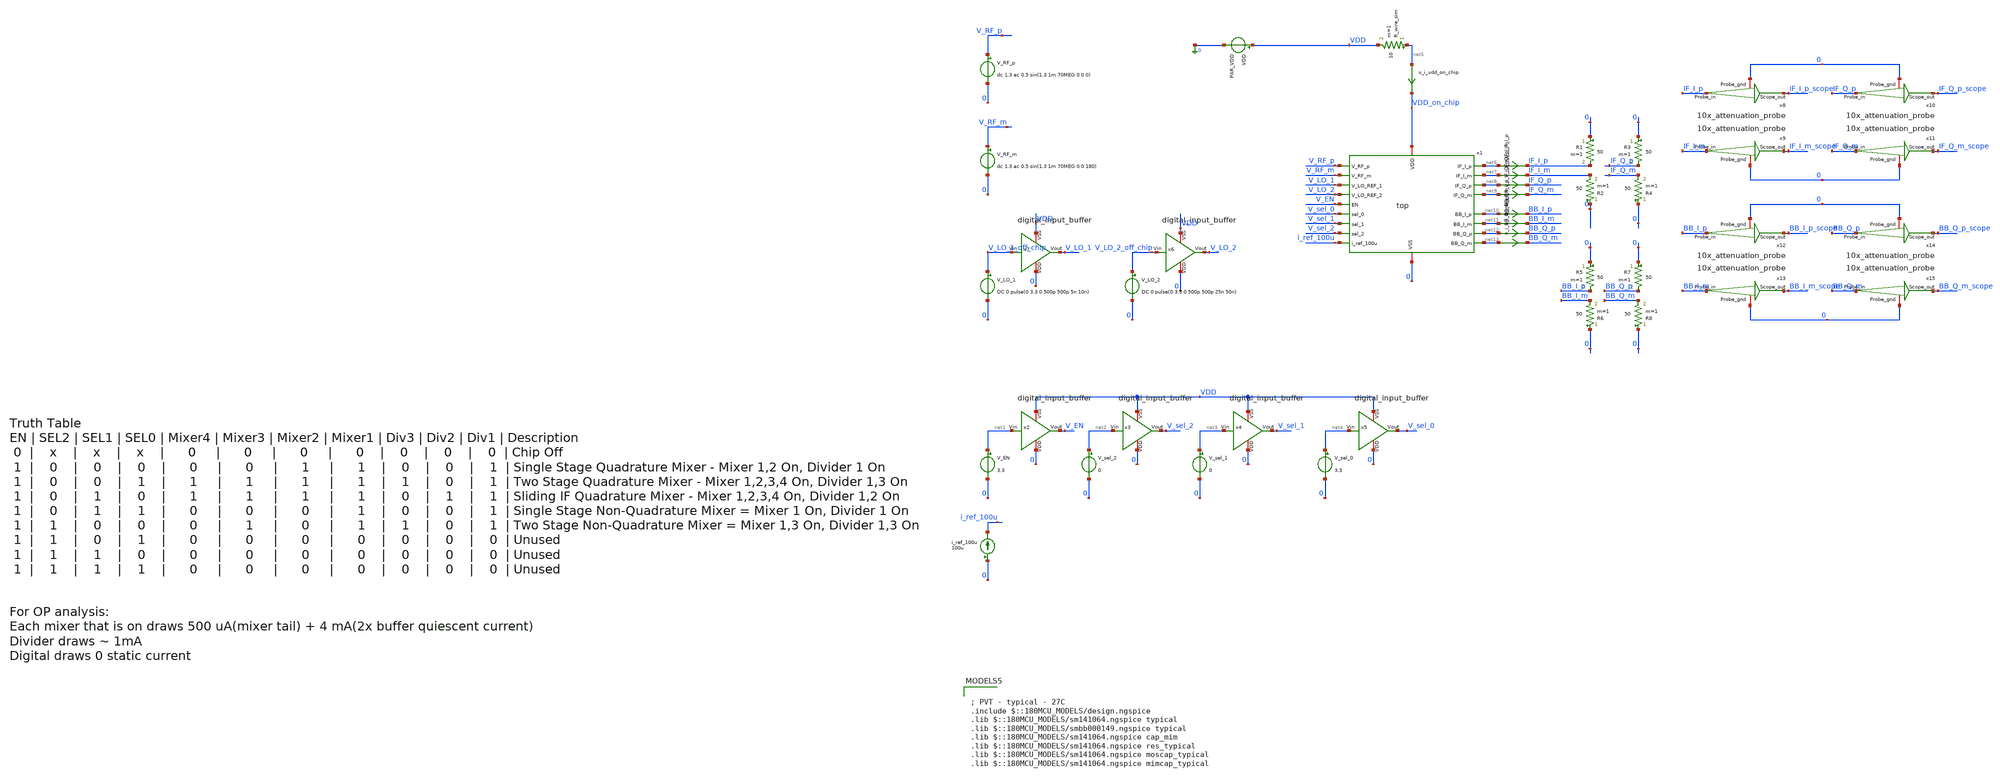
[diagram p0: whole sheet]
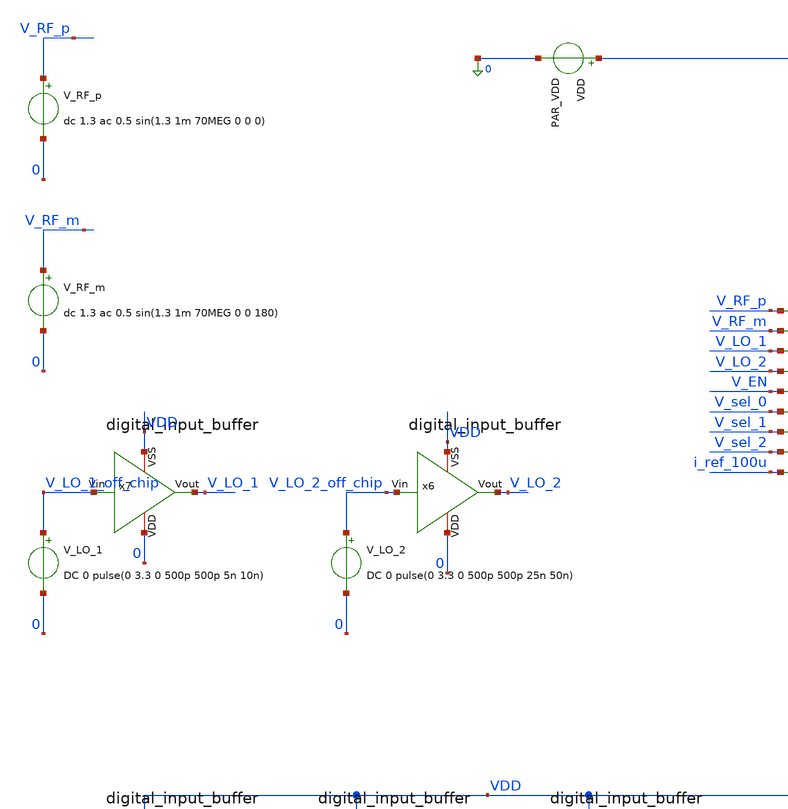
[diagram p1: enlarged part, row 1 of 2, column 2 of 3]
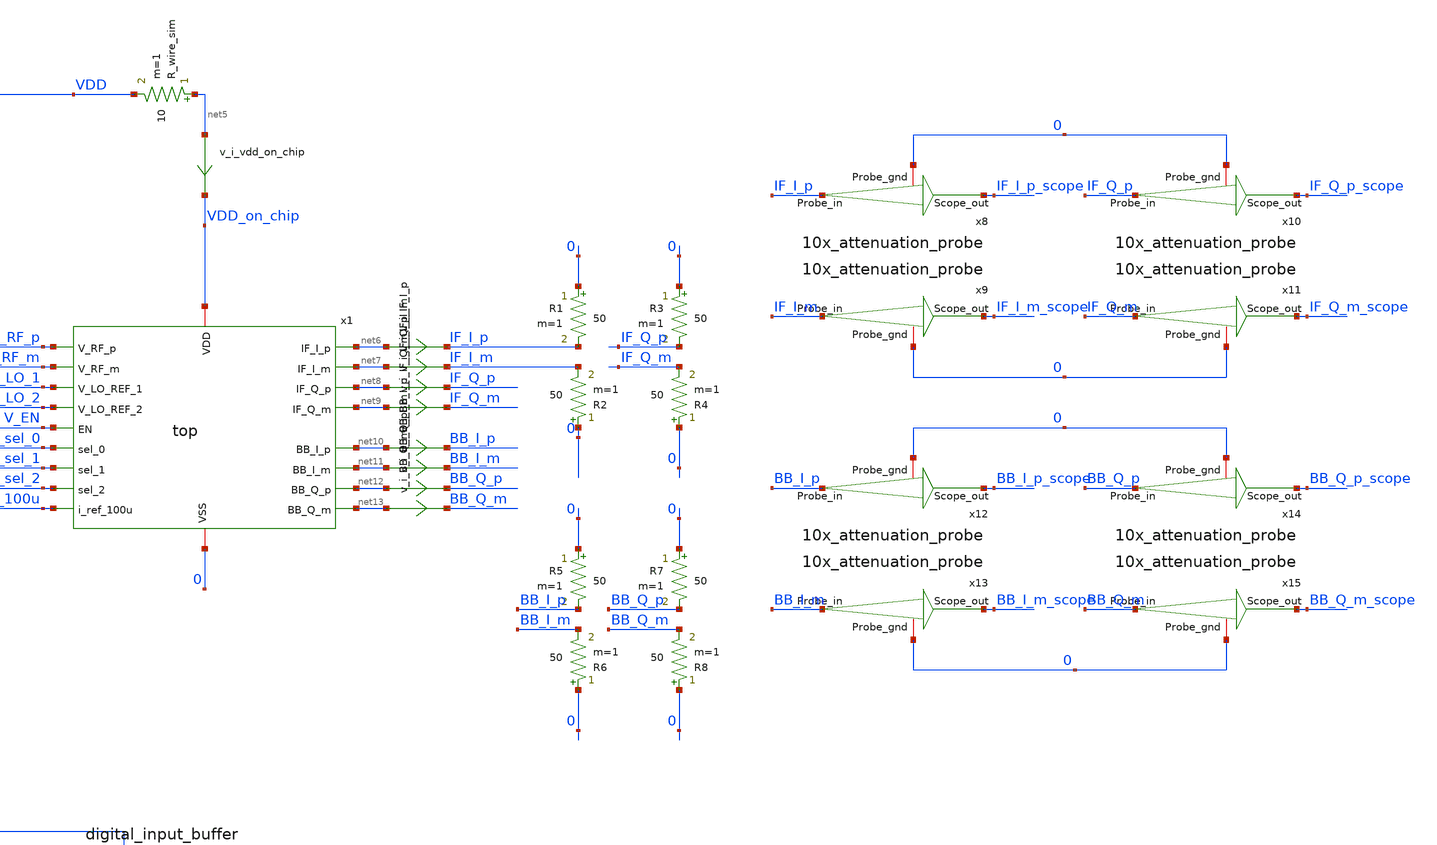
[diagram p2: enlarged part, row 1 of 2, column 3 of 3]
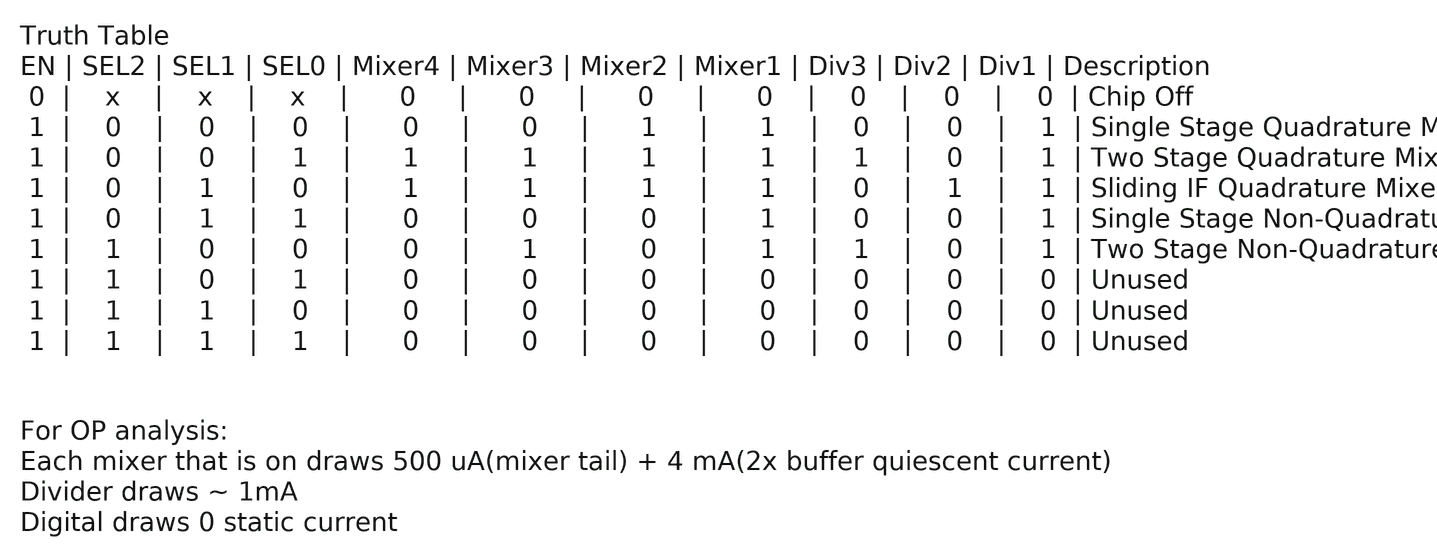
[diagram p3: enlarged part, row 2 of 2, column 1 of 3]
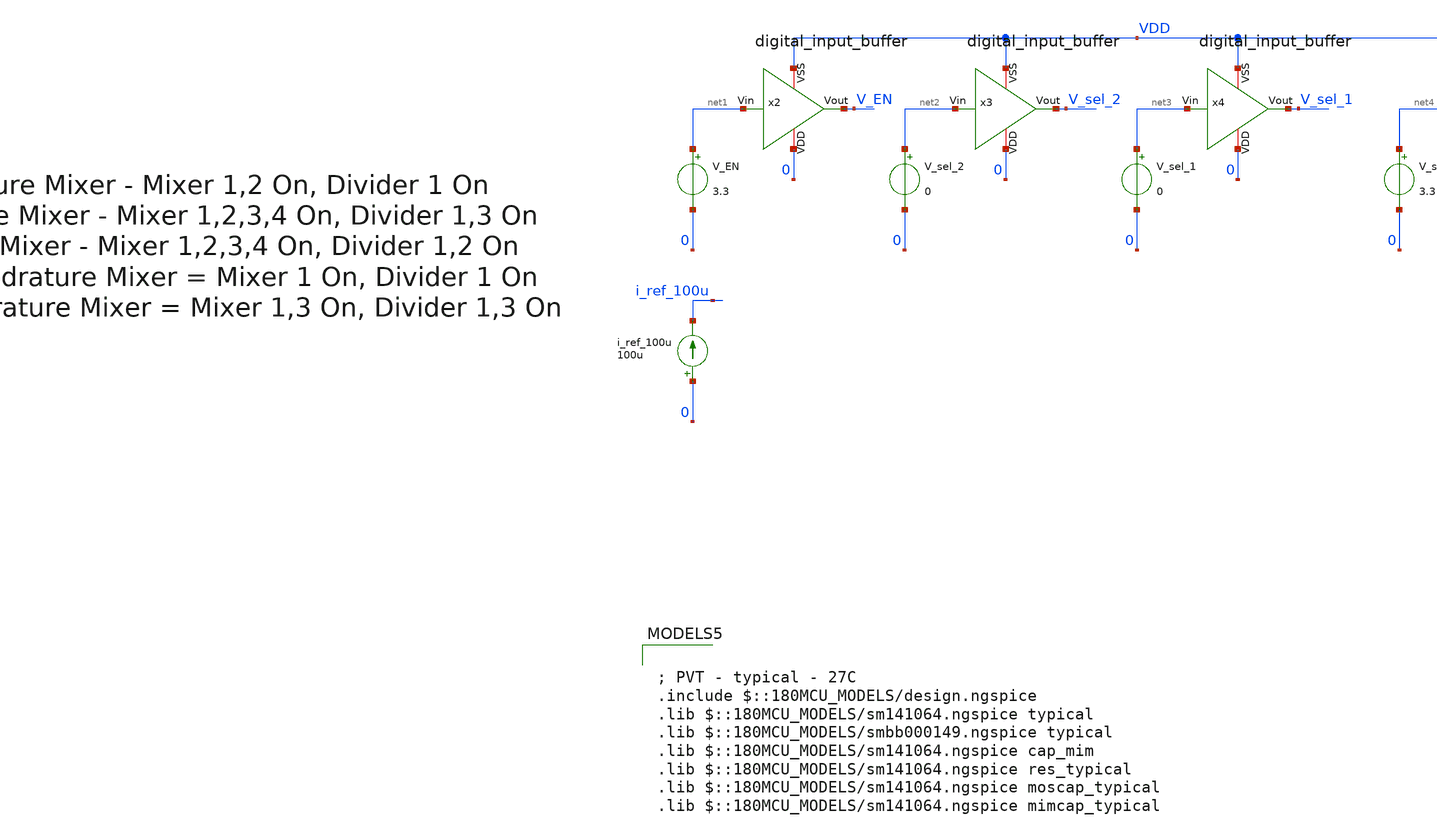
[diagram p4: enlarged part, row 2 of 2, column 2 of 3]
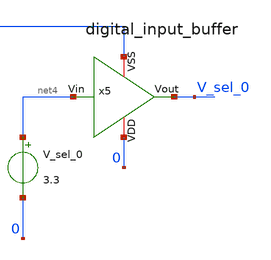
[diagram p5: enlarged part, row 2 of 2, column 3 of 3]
** sch_path: designs/top_level/testbench/tb_top.sch
**.subckt tb_top
x1 V_RF_p VDD_on_chip V_RF_m 0 V_LO_1 net6 net7 V_LO_2 net8 V_EN net9 V_sel_0 V_sel_1 net10 V_sel_2
+ net11 net12 i_ref_100u net13 top
VDD VDD 0 PAR_VDD
V_RF_p V_RF_p 0 dc 1.3 ac 0.5 sin(1.3 1m 70MEG 0 0 0)
R_wire_sim net5 VDD 10 m=1
V_RF_m V_RF_m 0 dc 1.3 ac 0.5 sin(1.3 1m 70MEG 0 0 180)
V_LO_1 V_LO_1_off_chip 0 DC 0 pulse(0 3.3 0 500p 500p 5n 10n)
V_LO_2 V_LO_2_off_chip 0 DC 0 pulse(0 3.3 0 500p 500p 25n 50n)
V_EN net1 0 3.3
V_sel_2 net2 0 0
V_sel_1 net3 0 0
V_sel_0 net4 0 3.3
i_ref_100u 0 i_ref_100u 100u
x2 VDD net1 V_EN 0 digital_input_buffer
x3 VDD net2 V_sel_2 0 digital_input_buffer
x4 VDD net3 V_sel_1 0 digital_input_buffer
x5 VDD net4 V_sel_0 0 digital_input_buffer
x6 VDD V_LO_2_off_chip V_LO_2 0 digital_input_buffer
x7 VDD V_LO_1_off_chip V_LO_1 0 digital_input_buffer
x8 IF_I_p IF_I_p_scope 0 10x_attenuation_probe
x9 IF_I_m IF_I_m_scope 0 10x_attenuation_probe
x10 IF_Q_p IF_Q_p_scope 0 10x_attenuation_probe
x11 IF_Q_m IF_Q_m_scope 0 10x_attenuation_probe
x12 BB_I_p BB_I_p_scope 0 10x_attenuation_probe
x13 BB_I_m BB_I_m_scope 0 10x_attenuation_probe
x14 BB_Q_p BB_Q_p_scope 0 10x_attenuation_probe
x15 BB_Q_m BB_Q_m_scope 0 10x_attenuation_probe
v_i_vdd_on_chip net5 VDD_on_chip 0
.save i(v_i_vdd_on_chip)
v_i_IF_I_p net6 IF_I_p 0
.save i(v_i_if_i_p)
v_i_IF_I_m net7 IF_I_m 0
.save i(v_i_if_i_m)
v_i_IF_Q_p net8 IF_Q_p 0
.save i(v_i_if_q_p)
v_i_IF_Q_m net9 IF_Q_m 0
.save i(v_i_if_q_m)
v_i_BB_I_p net10 BB_I_p 0
.save i(v_i_bb_i_p)
v_i_BB_I_m net11 BB_I_m 0
.save i(v_i_bb_i_m)
v_i_BB_Q_p net12 BB_Q_p 0
.save i(v_i_bb_q_p)
v_i_BB_Q_m net13 BB_Q_m 0
.save i(v_i_bb_q_m)
R1 0 IF_I_p 50 m=1
R2 0 IF_I_m 50 m=1
R3 0 IF_Q_p 50 m=1
R4 0 IF_Q_m 50 m=1
R5 0 BB_I_p 50 m=1
R6 0 BB_I_m 50 m=1
R7 0 BB_Q_p 50 m=1
R8 0 BB_Q_m 50 m=1
**** begin user architecture code

; PVT - typical - 27C
.include $::180MCU_MODELS/design.ngspice
.lib $::180MCU_MODELS/sm141064.ngspice typical
.lib $::180MCU_MODELS/smbb000149.ngspice typical
.lib $::180MCU_MODELS/sm141064.ngspice cap_mim
.lib $::180MCU_MODELS/sm141064.ngspice res_typical
.lib $::180MCU_MODELS/sm141064.ngspice moscap_typical
.lib $::180MCU_MODELS/sm141064.ngspice mimcap_typical



** PARAMS

.PARAM PAR_VDD=3.3

.control
destroy all
save all

write tb_top.raw

; 70Mhz input, 100 MHz LO REF 1, 20 MHz LO REF 2

tran .1n 2u

let vrf = V_rf_p - V_rf_m
let vif_i = if_i_p - if_i_m
let vif_q = if_q_p - if_q_m
let vbb_i = bb_i_p - bb_i_m
let vbb_q = bb_q_p - bb_q_m
let v_lo_1_i = x1.div_1_lo_i_p-x1.div_1_lo_i_m
let v_lo_1_q = x1.div_1_lo_q_p-x1.div_1_lo_q_m
let v_lo_3_i = x1.div_3_lo_i_p-x1.div_3_lo_i_m
let v_lo_3_q = x1.div_3_lo_q_p-x1.div_3_lo_q_m

plot vrf   ;input signal
plot vif_i vif_q xlimit 0 200n;output output
plot vbb_i vbb_q xlimit 0 200n;baseband output
plot v_lo_1 v_lo_1_off_chip x1.div_1_lo_i_p-x1.div_1_lo_i_m xlimit 0 200n;clock divider 1
plot v_lo_2 v_lo_2_off_chip x1.div_3_lo_i_p-x1.div_3_lo_i_m xlimit 0 200n;clock divider 2
plot x1.mix_3_4_lo_i_p x1.div_3_lo_i_p x1.mix_3_4_lo_q_p x1.div_3_lo_q_p ; actual clock input signal

meas tran i_vdd avg i(v_i_vdd_on_chip) from=.3u to=2u ;average vdd current from .3us to 2us
meas tran i_mix_1 avg i(v.x1.v_i_mix_1) from=.3u to=2u ;average mixer 1 current from .3us to 2us
meas tran i_mix_2 avg i(v.x1.v_i_mix_2) from=.3u to=2u ;average mixer 2 current from .3us to 2us
meas tran i_mix_3 avg i(v.x1.v_i_mix_3) from=.3u to=2u ;average mixer 3 current from .3us to 2us
meas tran i_mix_4 avg i(v.x1.v_i_mix_4) from=.3u to=2u ;average mixer 4 current from .3us to 2us
meas tran i_buf_mix_1_p avg i(v.x1.v_i_buf_mix_1_p) from=.3u to=2u ;average buffer current from .3us
+ to 2us
meas tran i_buf_mix_1_m avg i(v.x1.v_i_buf_mix_1_m) from=.3u to=2u ;average buffer current from .3us
+ to 2us
meas tran i_buf_mix_2_p avg i(v.x1.v_i_buf_mix_2_p) from=.3u to=2u ;average buffer current from .3us
+ to 2us
meas tran i_buf_mix_2_m avg i(v.x1.v_i_buf_mix_2_m) from=.3u to=2u ;average buffer current from .3us
+ to 2us
meas tran i_buf_mix_3_p avg i(v.x1.v_i_buf_mix_3_p) from=.3u to=2u ;average buffer current from .3us
+ to 2us
meas tran i_buf_mix_3_m avg i(v.x1.v_i_buf_mix_3_m) from=.3u to=2u ;average buffer current from .3us
+ to 2us
meas tran i_buf_mix_4_p avg i(v.x1.v_i_buf_mix_4_p) from=.3u to=2u ;average buffer current from .3us
+ to 2us
meas tran i_buf_mix_4_m avg i(v.x1.v_i_buf_mix_4_m) from=.3u to=2u ;average buffer current from .3us
+ to 2us

plot avg(i(v_i_vdd_on_chip)) i(v.x1.v_i_mix_1) i(v.x1.v_i_mix_2) i(v.x1.v_i_mix_3) i(v.x1.v_i_mix_4)
+ i(v.x1.v_i_buf_mix_1_p) i(v.x1.v_i_buf_mix_1_m) i(v.x1.v_i_buf_mix_2_p) i(v.x1.v_i_buf_mix_2_m) i(v.x1.v_i_buf_mix_3_p)
+ i(v.x1.v_i_buf_mix_3_m) i(v.x1.v_i_buf_mix_4_p) i(v.x1.v_i_buf_mix_4_m); current in active blocks

print i_vdd
print i_mix_1
print i_mix_2
print i_mix_3
print i_mix_4
print i_buf_mix_1_p
print i_buf_mix_1_m
print i_buf_mix_2_p
print i_buf_mix_2_m
print i_buf_mix_3_p
print i_buf_mix_3_m
print i_buf_mix_4_p
print i_buf_mix_4_m

let i_blocks =
+ i_mix_1+i_mix_2+i_mix_3+i_mix_4+i_buf_mix_1_p+i_buf_mix_1_m+i_buf_mix_2_p+i_buf_mix_2_m+i_buf_mix_3_p+i_buf_mix_3_m+i_buf_mix_4_p+i_buf_mix_4_m
print i_vdd-i_blocks

linearize vrf vif_i vif_q vbb_i vbb_q v_lo_1 v_lo_1_off_chip x1.div_1_lo_i_p x1.div_1_lo_i_m v_lo_2
+ v_lo_2_off_chip x1.div_3_lo_i_p x1.div_3_lo_i_m v_lo_1_i v_lo_1_q
fft vrf vif_i vif_q vbb_i vbb_q v_lo_1 v_lo_1_off_chip x1.div_1_lo_i_p x1.div_1_lo_i_m v_lo_2
+ v_lo_2_off_chip x1.div_3_lo_i_p x1.div_3_lo_i_m v_lo_1_i v_lo_1_q

;plot db(vrf) xlimit 1 200Meg; input signal
plot db(vrf) db(vif_i) db(vif_q) xlimit 1 200MEG; IF output
plot db(vrf) db(vbb_i) db(vbb_q) xlimit 1 200MEG; BB output
plot db(v_lo_1_off_chip) db(x1.div_1_lo_i_p) xlimit 1 200MEG;
plot db(v_lo_2_off_chip) db(x1.div_3_lo_i_p) xlimit 1 200MEG;
plot db(v_lo_1_i) db(v_lo_1_q); difference between I/Q LO 1 signal

.endc


**** end user architecture code
**.ends
.end
